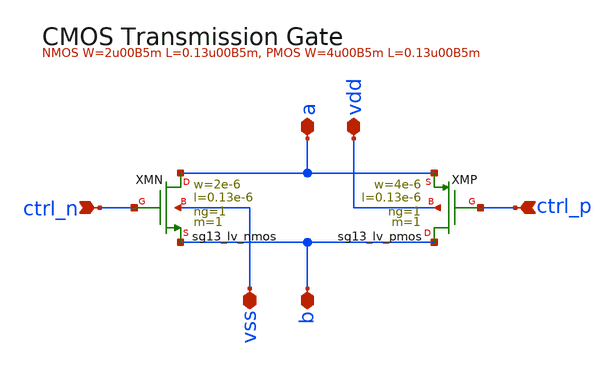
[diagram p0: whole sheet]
** sch_path: xschem/cmos_tg.sch
**.subckt cmos_tg a b ctrl_p vss vdd ctrl_n
*.iopin a
*.iopin b
*.ipin ctrl_p
*.iopin vss
*.iopin vdd
*.ipin ctrl_n
XXMN a ctrl_n b vss sg13_lv_nmos w=2e-6 l=0.13e-6 ng=1 m=1 mm_ok=1
XXMP b ctrl_p a vdd sg13_lv_pmos w=4e-6 l=0.13e-6 ng=1 m=1 mm_ok=1
**.ends
.end
